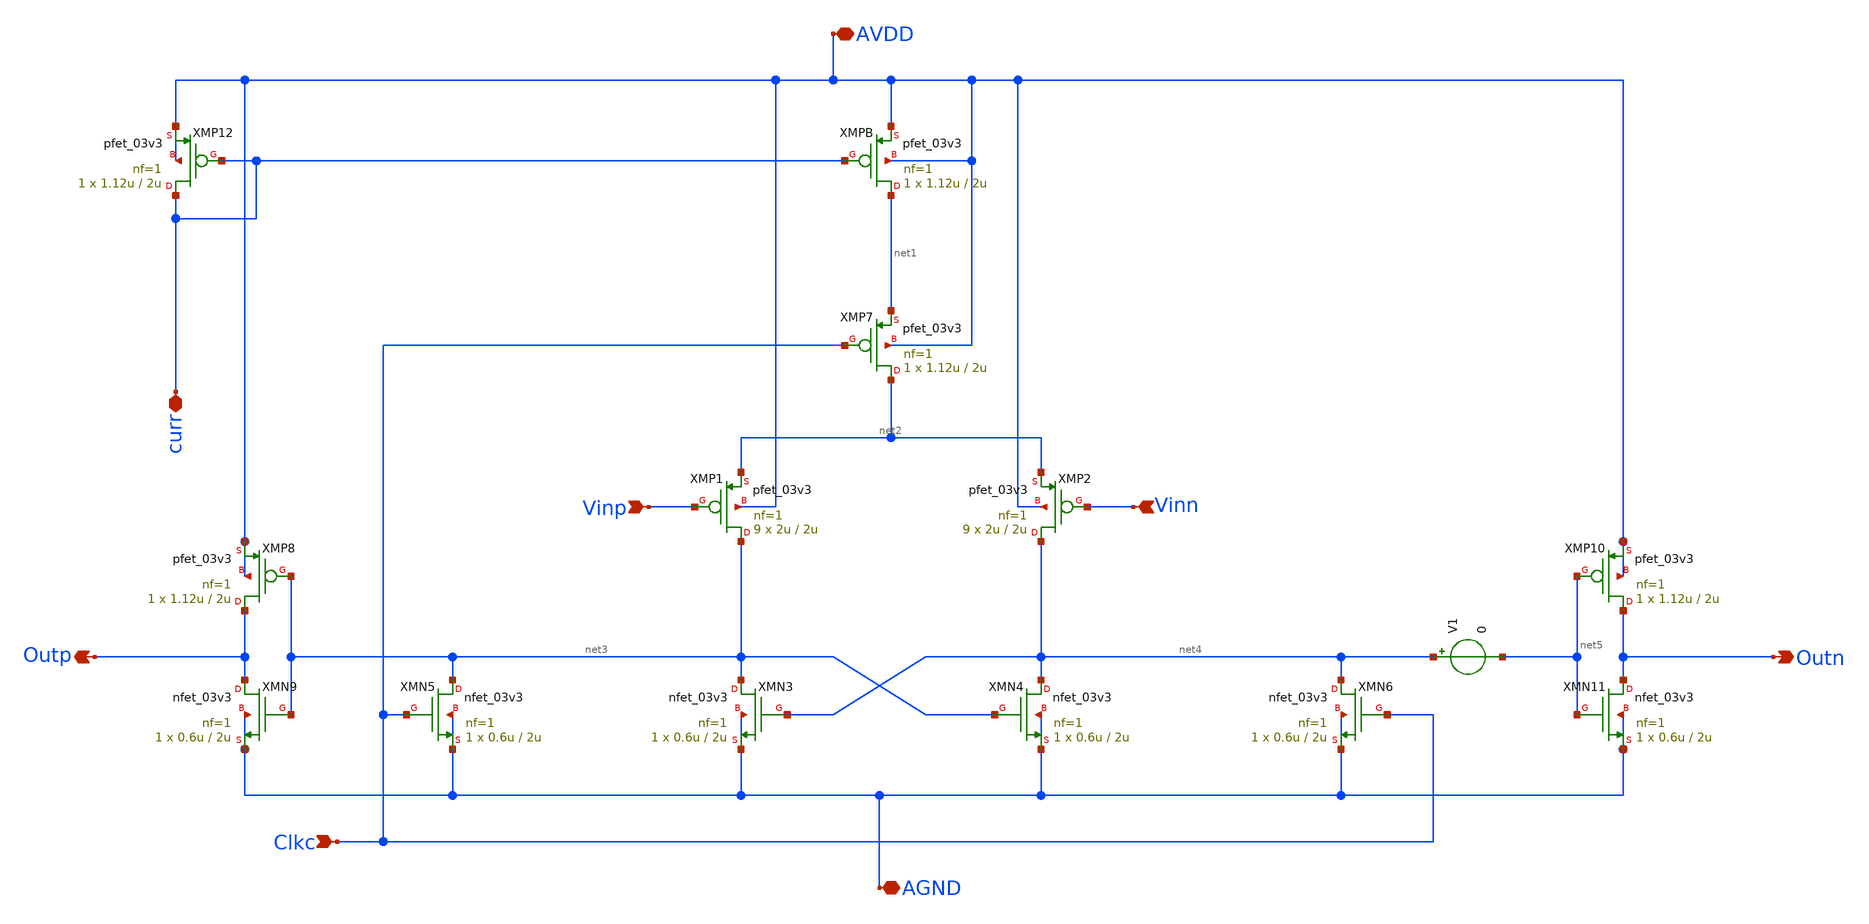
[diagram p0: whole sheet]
** sch_path: xschem/dyanamic_comp.sch
**.subckt dyanamic_comp AVDD curr Outp Clkc AGND Outn Vinp Vinn
*.iopin AVDD
*.iopin curr
*.opin Outp
*.ipin Clkc
*.iopin AGND
*.opin Outn
*.ipin Vinp
*.ipin Vinn
XMP1 net3 Vinp net2 AVDD pfet_03v3 L=2u W=2u nf=1 ad='int((nf+1)/2) * W/nf * 0.18u' as='int((nf+2)/2) * W/nf * 0.18u'
+ pd='2*int((nf+1)/2) * (W/nf + 0.18u)' ps='2*int((nf+2)/2) * (W/nf + 0.18u)' nrd='0.18u / W' nrs='0.18u / W'
+ sa=0 sb=0 sd=0 m=9
XMP2 net4 Vinn net2 AVDD pfet_03v3 L=2u W=2u nf=1 ad='int((nf+1)/2) * W/nf * 0.18u' as='int((nf+2)/2) * W/nf * 0.18u'
+ pd='2*int((nf+1)/2) * (W/nf + 0.18u)' ps='2*int((nf+2)/2) * (W/nf + 0.18u)' nrd='0.18u / W' nrs='0.18u / W'
+ sa=0 sb=0 sd=0 m=9
XMN4 net4 net3 AGND AGND nfet_03v3 L=2u W=0.6u nf=1 ad='int((nf+1)/2) * W/nf * 0.18u' as='int((nf+2)/2) * W/nf * 0.18u'
+ pd='2*int((nf+1)/2) * (W/nf + 0.18u)' ps='2*int((nf+2)/2) * (W/nf + 0.18u)' nrd='0.18u / W' nrs='0.18u / W'
+ sa=0 sb=0 sd=0 m=1
XMN5 net3 Clkc AGND AGND nfet_03v3 L=2u W=0.6u nf=1 ad='int((nf+1)/2) * W/nf * 0.18u' as='int((nf+2)/2) * W/nf * 0.18u'
+ pd='2*int((nf+1)/2) * (W/nf + 0.18u)' ps='2*int((nf+2)/2) * (W/nf + 0.18u)' nrd='0.18u / W' nrs='0.18u / W'
+ sa=0 sb=0 sd=0 m=1
XMN6 net4 Clkc AGND AGND nfet_03v3 L=2u W=0.6u nf=1 ad='int((nf+1)/2) * W/nf * 0.18u' as='int((nf+2)/2) * W/nf * 0.18u'
+ pd='2*int((nf+1)/2) * (W/nf + 0.18u)' ps='2*int((nf+2)/2) * (W/nf + 0.18u)' nrd='0.18u / W' nrs='0.18u / W'
+ sa=0 sb=0 sd=0 m=1
XMN3 net3 net4 AGND AGND nfet_03v3 L=2u W=0.6u nf=1 ad='int((nf+1)/2) * W/nf * 0.18u' as='int((nf+2)/2) * W/nf * 0.18u'
+ pd='2*int((nf+1)/2) * (W/nf + 0.18u)' ps='2*int((nf+2)/2) * (W/nf + 0.18u)' nrd='0.18u / W' nrs='0.18u / W'
+ sa=0 sb=0 sd=0 m=1
XMP7 net2 Clkc net1 AVDD pfet_03v3 L=2u W=1.12u nf=1 ad='int((nf+1)/2) * W/nf * 0.18u' as='int((nf+2)/2) * W/nf * 0.18u'
+ pd='2*int((nf+1)/2) * (W/nf + 0.18u)' ps='2*int((nf+2)/2) * (W/nf + 0.18u)' nrd='0.18u / W' nrs='0.18u / W'
+ sa=0 sb=0 sd=0 m=1
XMPB net1 curr AVDD AVDD pfet_03v3 L=2u W=1.12u nf=1 ad='int((nf+1)/2) * W/nf * 0.18u' as='int((nf+2)/2) * W/nf * 0.18u'
+ pd='2*int((nf+1)/2) * (W/nf + 0.18u)' ps='2*int((nf+2)/2) * (W/nf + 0.18u)' nrd='0.18u / W' nrs='0.18u / W'
+ sa=0 sb=0 sd=0 m=1
XMP12 curr curr AVDD AVDD pfet_03v3 L=2u W=1.12u nf=1 ad='int((nf+1)/2) * W/nf * 0.18u' as='int((nf+2)/2) * W/nf * 0.18u'
+ pd='2*int((nf+1)/2) * (W/nf + 0.18u)' ps='2*int((nf+2)/2) * (W/nf + 0.18u)' nrd='0.18u / W' nrs='0.18u / W'
+ sa=0 sb=0 sd=0 m=1
XMP10 Outn net5 AVDD AVDD pfet_03v3 L=2u W=1.12u nf=1 ad='int((nf+1)/2) * W/nf * 0.18u' as='int((nf+2)/2) * W/nf * 0.18u'
+ pd='2*int((nf+1)/2) * (W/nf + 0.18u)' ps='2*int((nf+2)/2) * (W/nf + 0.18u)' nrd='0.18u / W' nrs='0.18u / W'
+ sa=0 sb=0 sd=0 m=1
XMN11 Outn net5 AGND AGND nfet_03v3 L=2u W=0.6u nf=1 ad='int((nf+1)/2) * W/nf * 0.18u' as='int((nf+2)/2) * W/nf * 0.18u'
+ pd='2*int((nf+1)/2) * (W/nf + 0.18u)' ps='2*int((nf+2)/2) * (W/nf + 0.18u)' nrd='0.18u / W' nrs='0.18u / W'
+ sa=0 sb=0 sd=0 m=1
XMP8 Outp net3 AVDD AVDD pfet_03v3 L=2u W=1.12u nf=1 ad='int((nf+1)/2) * W/nf * 0.18u' as='int((nf+2)/2) * W/nf * 0.18u'
+ pd='2*int((nf+1)/2) * (W/nf + 0.18u)' ps='2*int((nf+2)/2) * (W/nf + 0.18u)' nrd='0.18u / W' nrs='0.18u / W'
+ sa=0 sb=0 sd=0 m=1
XMN9 Outp net3 AGND AGND nfet_03v3 L=2u W=0.6u nf=1 ad='int((nf+1)/2) * W/nf * 0.18u' as='int((nf+2)/2) * W/nf * 0.18u'
+ pd='2*int((nf+1)/2) * (W/nf + 0.18u)' ps='2*int((nf+2)/2) * (W/nf + 0.18u)' nrd='0.18u / W' nrs='0.18u / W'
+ sa=0 sb=0 sd=0 m=1
V1 net4 net5 0
**.ends
.end
